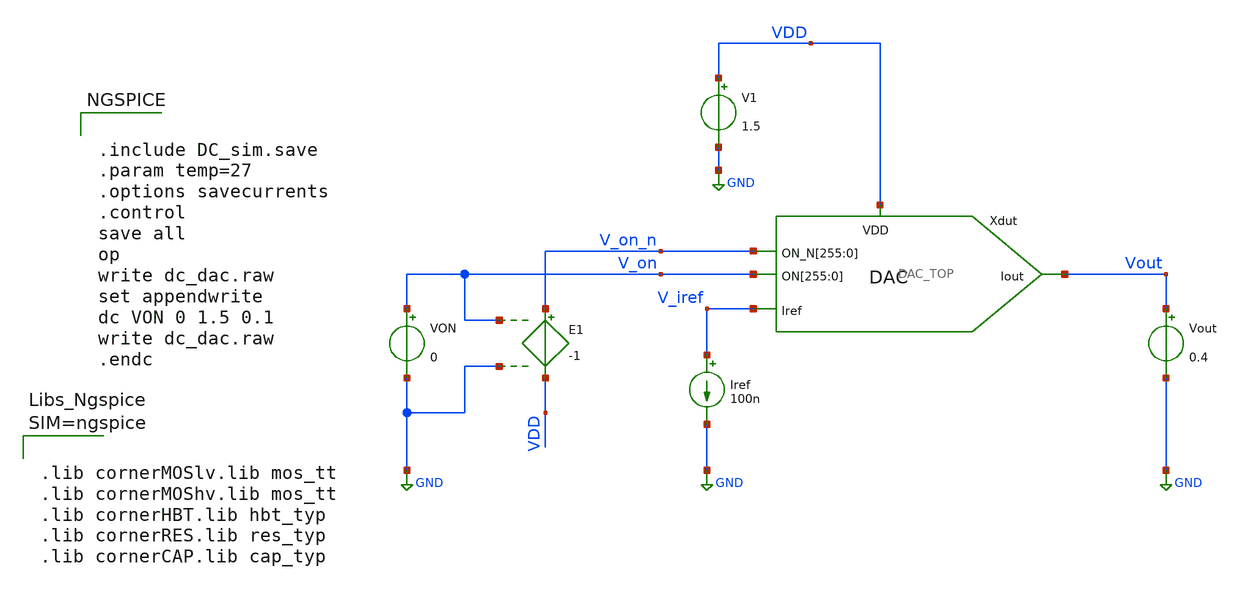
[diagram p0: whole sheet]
** sch_path: xschem/DC_sim.sch
**.subckt DC_sim
Xdut VDD V_on V_on V_on V_on V_on V_on V_on V_on V_on V_on V_on V_on V_on V_on V_on V_on V_on V_on
+ V_on V_on V_on V_on V_on V_on V_on V_on V_on V_on V_on V_on V_on V_on V_on V_on V_on V_on V_on V_on V_on
+ V_on V_on V_on V_on V_on V_on V_on V_on V_on V_on V_on V_on V_on V_on V_on V_on V_on V_on V_on V_on V_on
+ V_on V_on V_on V_on V_on V_on V_on V_on V_on V_on V_on V_on V_on V_on V_on V_on V_on V_on V_on V_on V_on
+ V_on V_on V_on V_on V_on V_on V_on V_on V_on V_on V_on V_on V_on V_on V_on V_on V_on V_on V_on V_on V_on
+ V_on V_on V_on V_on V_on V_on V_on V_on V_on V_on V_on V_on V_on V_on V_on V_on V_on V_on V_on V_on V_on
+ V_on V_on V_on V_on V_on V_on V_on V_on V_on V_on V_on V_on V_on V_on V_on V_on V_on V_on V_on V_on V_on
+ V_on V_on V_on V_on V_on V_on V_on V_on V_on V_on V_on V_on V_on V_on V_on V_on V_on V_on V_on V_on V_on
+ V_on V_on V_on V_on V_on V_on V_on V_on V_on V_on V_on V_on V_on V_on V_on V_on V_on V_on V_on V_on V_on
+ V_on V_on V_on V_on V_on V_on V_on V_on V_on V_on V_on V_on V_on V_on V_on V_on V_on V_on V_on V_on V_on
+ V_on V_on V_on V_on V_on V_on V_on V_on V_on V_on V_on V_on V_on V_on V_on V_on V_on V_on V_on V_on V_on
+ V_on V_on V_on V_on V_on V_on V_on V_on V_on V_on V_on V_on V_on V_on V_on V_on V_on V_on V_on V_on V_on
+ V_on V_on V_on V_on V_on V_on V_on Vout V_iref V_on_n V_on_n V_on_n V_on_n V_on_n V_on_n V_on_n V_on_n
+ V_on_n V_on_n V_on_n V_on_n V_on_n V_on_n V_on_n V_on_n V_on_n V_on_n V_on_n V_on_n V_on_n V_on_n V_on_n
+ V_on_n V_on_n V_on_n V_on_n V_on_n V_on_n V_on_n V_on_n V_on_n V_on_n V_on_n V_on_n V_on_n V_on_n V_on_n
+ V_on_n V_on_n V_on_n V_on_n V_on_n V_on_n V_on_n V_on_n V_on_n V_on_n V_on_n V_on_n V_on_n V_on_n V_on_n
+ V_on_n V_on_n V_on_n V_on_n V_on_n V_on_n V_on_n V_on_n V_on_n V_on_n V_on_n V_on_n V_on_n V_on_n V_on_n
+ V_on_n V_on_n V_on_n V_on_n V_on_n V_on_n V_on_n V_on_n V_on_n V_on_n V_on_n V_on_n V_on_n V_on_n V_on_n
+ V_on_n V_on_n V_on_n V_on_n V_on_n V_on_n V_on_n V_on_n V_on_n V_on_n V_on_n V_on_n V_on_n V_on_n V_on_n
+ V_on_n V_on_n V_on_n V_on_n V_on_n V_on_n V_on_n V_on_n V_on_n V_on_n V_on_n V_on_n V_on_n V_on_n V_on_n
+ V_on_n V_on_n V_on_n V_on_n V_on_n V_on_n V_on_n V_on_n V_on_n V_on_n V_on_n V_on_n V_on_n V_on_n V_on_n
+ V_on_n V_on_n V_on_n V_on_n V_on_n V_on_n V_on_n V_on_n V_on_n V_on_n V_on_n V_on_n V_on_n V_on_n V_on_n
+ V_on_n V_on_n V_on_n V_on_n V_on_n V_on_n V_on_n V_on_n V_on_n V_on_n V_on_n V_on_n V_on_n V_on_n V_on_n
+ V_on_n V_on_n V_on_n V_on_n V_on_n V_on_n V_on_n V_on_n V_on_n V_on_n V_on_n V_on_n V_on_n V_on_n V_on_n
+ V_on_n V_on_n V_on_n V_on_n V_on_n V_on_n V_on_n V_on_n V_on_n V_on_n V_on_n V_on_n V_on_n V_on_n V_on_n
+ V_on_n V_on_n V_on_n V_on_n V_on_n V_on_n V_on_n V_on_n V_on_n V_on_n V_on_n V_on_n V_on_n V_on_n V_on_n
+ V_on_n V_on_n V_on_n V_on_n V_on_n V_on_n V_on_n V_on_n V_on_n V_on_n V_on_n V_on_n V_on_n V_on_n V_on_n
+ V_on_n V_on_n V_on_n V_on_n V_on_n V_on_n V_on_n V_on_n V_on_n V_on_n V_on_n V_on_n V_on_n V_on_n V_on_n
+ V_on_n V_on_n V_on_n V_on_n V_on_n V_on_n V_on_n V_on_n V_on_n V_on_n V_on_n V_on_n V_on_n V_on_n V_on_n
+ V_on_n V_on_n V_on_n V_on_n V_on_n V_on_n V_on_n V_on_n DAC_TOP
V1 VDD GND 1.5
.save i(v1)
Vout Vout GND 0.4
.save i(vout)
Iref V_iref GND 100n
VON V_on GND 0
.save i(von)
E1 V_on_n VDD V_on GND -1
**** begin user architecture code


.include DC_sim.save
.param temp=27
.options savecurrents
.control
save all
op
write dc_dac.raw
set appendwrite
dc VON 0 1.5 0.1
write dc_dac.raw
.endc





.lib cornerMOSlv.lib mos_tt
.lib cornerMOShv.lib mos_tt
.lib cornerHBT.lib hbt_typ
.lib cornerRES.lib res_typ
.lib cornerCAP.lib cap_typ



**** end user architecture code
**.ends
.GLOBAL GND
.end
